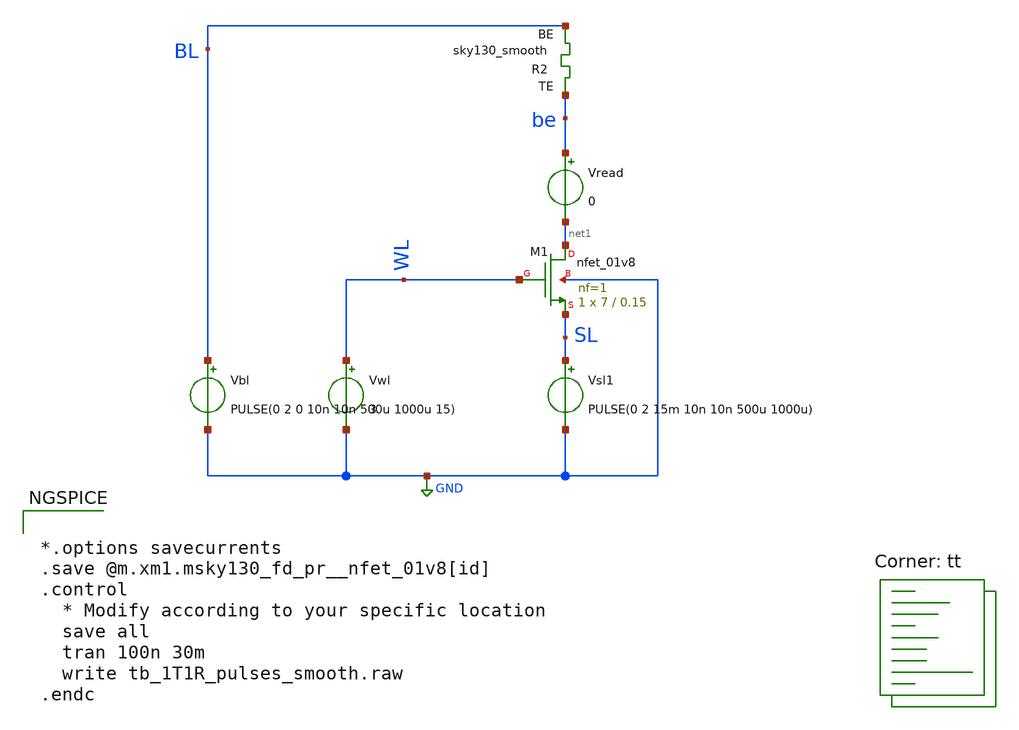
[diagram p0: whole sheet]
** sch_path: memristor_models/sky130_smooth/tb_1T1R_pulses_smooth.sch
**.subckt tb_1T1R_pulses_smooth
XM1 net1 WL SL GND sky130_fd_pr__nfet_01v8 L=0.15 W=7 nf=1 ad='int((nf+1)/2) * W/nf * 0.29' as='int((nf+2)/2) * W/nf * 0.29'
+ pd='2*int((nf+1)/2) * (W/nf + 0.29)' ps='2*int((nf+2)/2) * (W/nf + 0.29)' nrd='0.29 / W' nrs='0.29 / W'
+ sa=0 sb=0 sd=0 mult=1 m=1
Vwl WL GND 3
Vbl BL GND PULSE(0 2 0 10n 10n 500u 1000u 15)
Vread be net1 0
Vsl1 SL GND PULSE(0 2 15m 10n 10n 500u 1000u)
XR2 be BL sky130_smooth Tfilament_0=3.3e-9
**** begin user architecture code


*.options savecurrents
.save @m.xm1.msky130_fd_pr__nfet_01v8[id]
.control
  * Modify according to your specific location
  save all
  tran 100n 30m
  write tb_1T1R_pulses_smooth.raw
.endc



.lib $::SKYWATER_MODELS/sky130.lib.spice tt

** opencircuitdesign pdks install
.inc $::SKYWATER_MODELS/sky130_smooth.spice

**** end user architecture code
**.ends
.GLOBAL GND
.end
